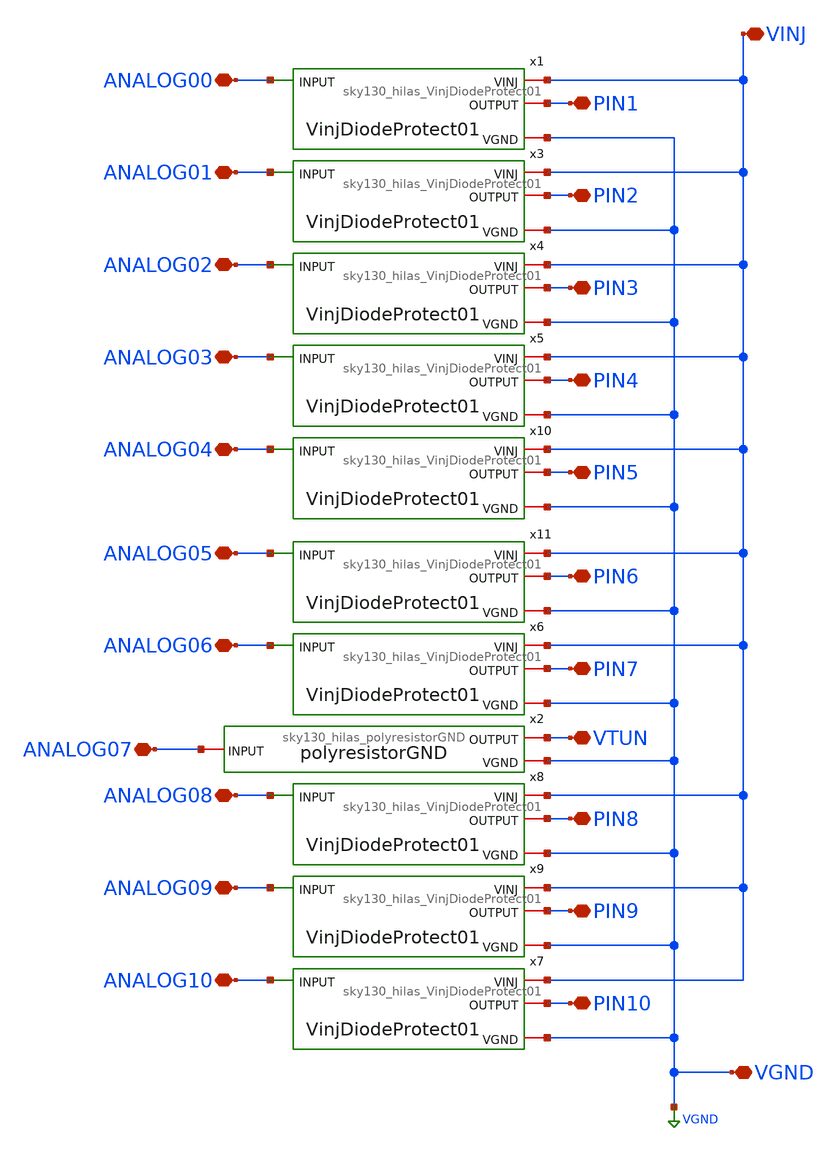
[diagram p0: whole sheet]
** sch_path: libs.ref/sky130_hilas_sc/xschem/sky130_hilas_TopProtection.sch
**.subckt sky130_hilas_TopProtection PIN1 ANALOG00 ANALOG01 VTUN ANALOG02 ANALOG03 ANALOG04 ANALOG05
*+ ANALOG06 ANALOG07 ANALOG08 ANALOG09 ANALOG10 PIN2 PIN3 PIN4 PIN5 PIN6 PIN7 PIN8 PIN9 PIN10 VINJ VGND
*.iopin PIN1
*.iopin ANALOG00
*.iopin ANALOG01
*.iopin VTUN
*.iopin ANALOG02
*.iopin ANALOG03
*.iopin ANALOG04
*.iopin ANALOG05
*.iopin ANALOG06
*.iopin ANALOG07
*.iopin ANALOG08
*.iopin ANALOG09
*.iopin ANALOG10
*.iopin PIN2
*.iopin PIN3
*.iopin PIN4
*.iopin PIN5
*.iopin PIN6
*.iopin PIN7
*.iopin PIN8
*.iopin PIN9
*.iopin PIN10
*.iopin VINJ
*.iopin VGND
x1 VINJ PIN1 ANALOG00 VGND sky130_hilas_VinjDiodeProtect01
x2 ANALOG07 VTUN VGND sky130_hilas_polyresistorGND
x3 VINJ PIN2 ANALOG01 VGND sky130_hilas_VinjDiodeProtect01
x4 VINJ PIN3 ANALOG02 VGND sky130_hilas_VinjDiodeProtect01
x5 VINJ PIN4 ANALOG03 VGND sky130_hilas_VinjDiodeProtect01
x6 VINJ PIN7 ANALOG06 VGND sky130_hilas_VinjDiodeProtect01
x7 VINJ PIN10 ANALOG10 VGND sky130_hilas_VinjDiodeProtect01
x8 VINJ PIN8 ANALOG08 VGND sky130_hilas_VinjDiodeProtect01
x9 VINJ PIN9 ANALOG09 VGND sky130_hilas_VinjDiodeProtect01
x10 VINJ PIN5 ANALOG04 VGND sky130_hilas_VinjDiodeProtect01
x11 VINJ PIN6 ANALOG05 VGND sky130_hilas_VinjDiodeProtect01
**.ends

* expanding   symbol:  sky130_hilas_VinjDiodeProtect01.sym # of pins=4
** sym_path: libs.ref/sky130_hilas_sc/xschem/sky130_hilas_VinjDiodeProtect01.sym
** sch_path: libs.ref/sky130_hilas_sc/xschem/sky130_hilas_VinjDiodeProtect01.sch
.subckt sky130_hilas_VinjDiodeProtect01 VINJ OUTPUT INPUT VGND
*.ipin INPUT
*.iopin VINJ
*.iopin OUTPUT
*.iopin VGND
XD1 OUTPUT VINJ sky130_fd_pr__diode_pw2nd_05v5 area=1 pj=4e6
XD2 VGND OUTPUT sky130_fd_pr__diode_pw2nd_05v5 area=1 pj=4e6
R1 INPUT OUTPUT 100 m=1
.ends


* expanding   symbol:  sky130_hilas_polyresistorGND.sym # of pins=3
** sym_path: libs.ref/sky130_hilas_sc/xschem/sky130_hilas_polyresistorGND.sym
** sch_path: libs.ref/sky130_hilas_sc/xschem/sky130_hilas_polyresistorGND.sch
.subckt sky130_hilas_polyresistorGND INPUT OUTPUT VGND
*.iopin OUTPUT
*.iopin VGND
*.iopin INPUT
R1 OUTPUT VGND 100k m=1
R2 INPUT OUTPUT 100 m=1
.ends

.GLOBAL VGND
.end
